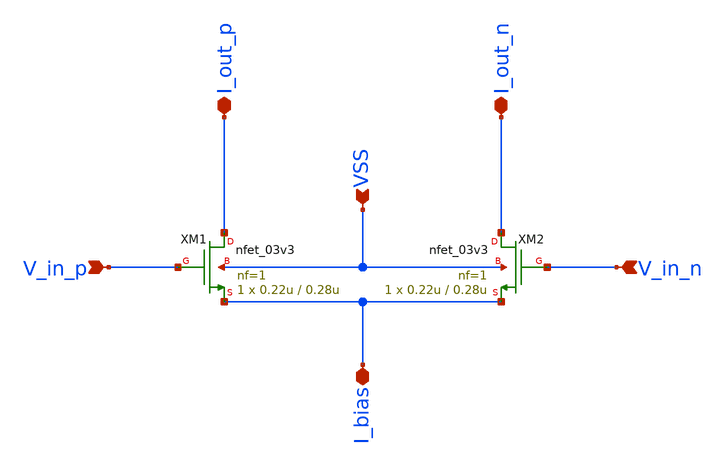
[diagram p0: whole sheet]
** sch_path: schematics/diff_pair.sch
**.subckt diff_pair V_in_p V_in_n VSS I_bias I_out_p I_out_n
*.ipin V_in_p
*.ipin V_in_n
*.ipin VSS
*.iopin I_bias
*.iopin I_out_p
*.iopin I_out_n
XM1 I_out_p V_in_p I_bias VSS nfet_03v3 L=0.28u W=0.22u nf=1 ad='int((nf+1)/2) * W/nf * 0.18u' as='int((nf+2)/2) * W/nf * 0.18u'
+ pd='2*int((nf+1)/2) * (W/nf + 0.18u)' ps='2*int((nf+2)/2) * (W/nf + 0.18u)' nrd='0.18u / W' nrs='0.18u / W'
+ sa=0 sb=0 sd=0 m=1
XM2 I_out_n V_in_n I_bias VSS nfet_03v3 L=0.28u W=0.22u nf=1 ad='int((nf+1)/2) * W/nf * 0.18u' as='int((nf+2)/2) * W/nf * 0.18u'
+ pd='2*int((nf+1)/2) * (W/nf + 0.18u)' ps='2*int((nf+2)/2) * (W/nf + 0.18u)' nrd='0.18u / W' nrs='0.18u / W'
+ sa=0 sb=0 sd=0 m=1
**.ends
.end
